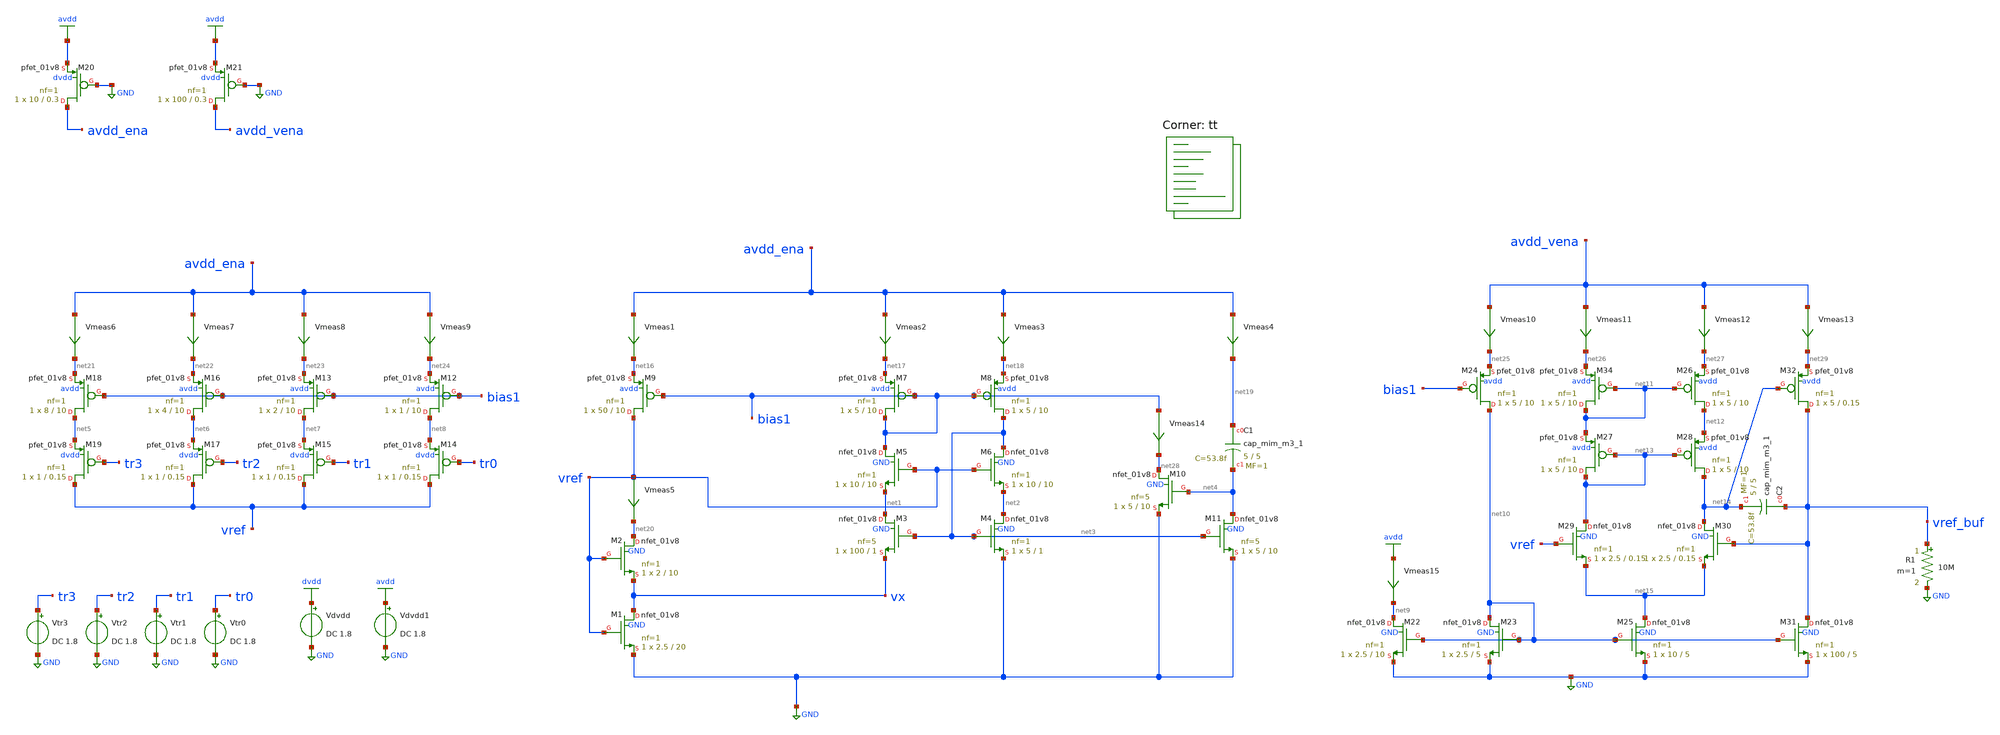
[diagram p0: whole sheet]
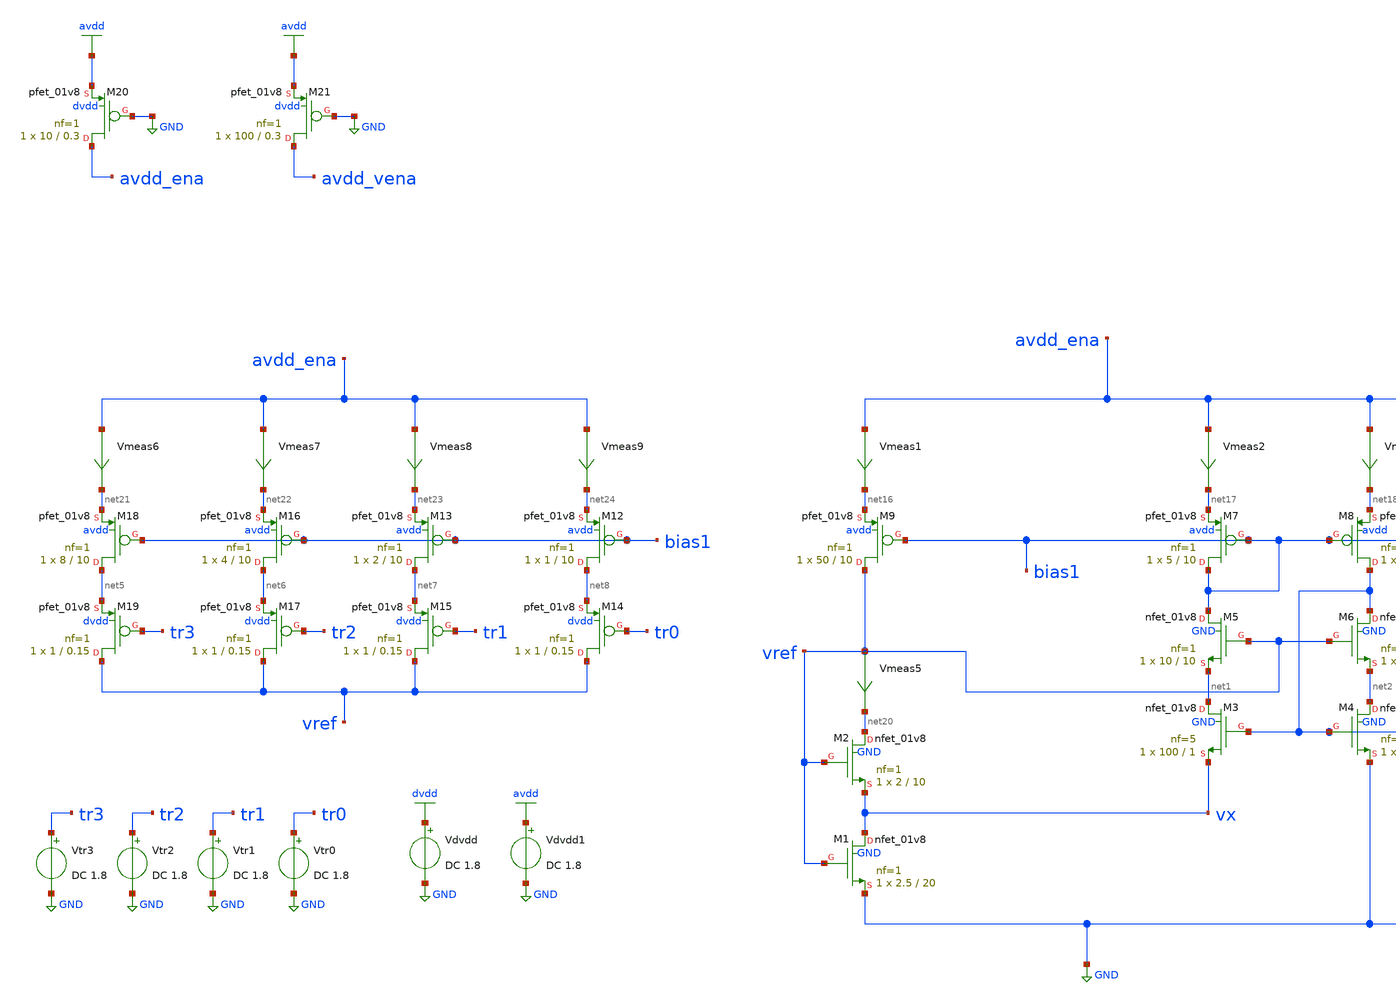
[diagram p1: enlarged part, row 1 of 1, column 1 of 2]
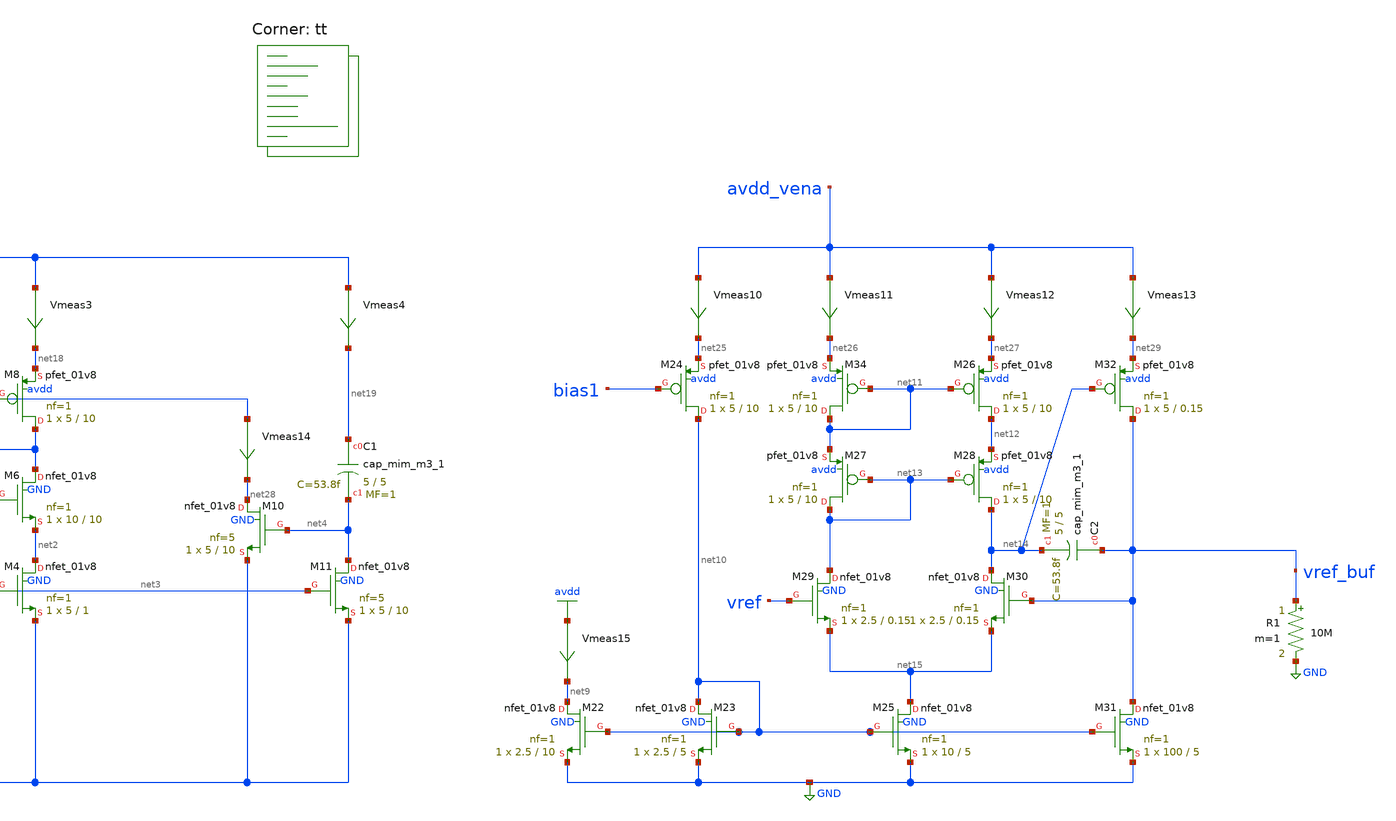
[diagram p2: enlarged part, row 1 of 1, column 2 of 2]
** sch_path: xschem/cmos_vref_design.sch
**.subckt cmos_vref_design
XM2 net20 vref vx GND sky130_fd_pr__nfet_01v8 L=10 W=2 nf=1 ad='int((nf+1)/2) * W/nf * 0.29' as='int((nf+2)/2) * W/nf * 0.29'
+ pd='2*int((nf+1)/2) * (W/nf + 0.29)' ps='2*int((nf+2)/2) * (W/nf + 0.29)' nrd='0.29 / W' nrs='0.29 / W'
+ sa=0 sb=0 sd=0 mult=1 m=1
XM1 vx vref GND GND sky130_fd_pr__nfet_01v8 L=20 W=2.5 nf=1 ad='int((nf+1)/2) * W/nf * 0.29' as='int((nf+2)/2) * W/nf * 0.29'
+ pd='2*int((nf+1)/2) * (W/nf + 0.29)' ps='2*int((nf+2)/2) * (W/nf + 0.29)' nrd='0.29 / W' nrs='0.29 / W'
+ sa=0 sb=0 sd=0 mult=1 m=1
XM3 net1 net3 vx GND sky130_fd_pr__nfet_01v8 L=1 W=100 nf=5 ad='int((nf+1)/2) * W/nf * 0.29' as='int((nf+2)/2) * W/nf * 0.29'
+ pd='2*int((nf+1)/2) * (W/nf + 0.29)' ps='2*int((nf+2)/2) * (W/nf + 0.29)' nrd='0.29 / W' nrs='0.29 / W'
+ sa=0 sb=0 sd=0 mult=1 m=1
XM4 net2 net3 GND GND sky130_fd_pr__nfet_01v8 L=1 W=5 nf=1 ad='int((nf+1)/2) * W/nf * 0.29' as='int((nf+2)/2) * W/nf * 0.29'
+ pd='2*int((nf+1)/2) * (W/nf + 0.29)' ps='2*int((nf+2)/2) * (W/nf + 0.29)' nrd='0.29 / W' nrs='0.29 / W'
+ sa=0 sb=0 sd=0 mult=1 m=1
XM5 bias1 vref net1 GND sky130_fd_pr__nfet_01v8 L=10 W=10 nf=1 ad='int((nf+1)/2) * W/nf * 0.29' as='int((nf+2)/2) * W/nf * 0.29'
+ pd='2*int((nf+1)/2) * (W/nf + 0.29)' ps='2*int((nf+2)/2) * (W/nf + 0.29)' nrd='0.29 / W' nrs='0.29 / W'
+ sa=0 sb=0 sd=0 mult=1 m=1
XM6 net3 vref net2 GND sky130_fd_pr__nfet_01v8 L=10 W=10 nf=1 ad='int((nf+1)/2) * W/nf * 0.29' as='int((nf+2)/2) * W/nf * 0.29'
+ pd='2*int((nf+1)/2) * (W/nf + 0.29)' ps='2*int((nf+2)/2) * (W/nf + 0.29)' nrd='0.29 / W' nrs='0.29 / W'
+ sa=0 sb=0 sd=0 mult=1 m=1
XM7 bias1 bias1 net17 avdd sky130_fd_pr__pfet_01v8 L=10 W=5 nf=1 ad='int((nf+1)/2) * W/nf * 0.29' as='int((nf+2)/2) * W/nf * 0.29'
+ pd='2*int((nf+1)/2) * (W/nf + 0.29)' ps='2*int((nf+2)/2) * (W/nf + 0.29)' nrd='0.29 / W' nrs='0.29 / W'
+ sa=0 sb=0 sd=0 mult=1 m=1
XM8 net3 bias1 net18 avdd sky130_fd_pr__pfet_01v8 L=10 W=5 nf=1 ad='int((nf+1)/2) * W/nf * 0.29' as='int((nf+2)/2) * W/nf * 0.29'
+ pd='2*int((nf+1)/2) * (W/nf + 0.29)' ps='2*int((nf+2)/2) * (W/nf + 0.29)' nrd='0.29 / W' nrs='0.29 / W'
+ sa=0 sb=0 sd=0 mult=1 m=1
XM9 vref bias1 net16 avdd sky130_fd_pr__pfet_01v8 L=10 W=50 nf=1 ad='int((nf+1)/2) * W/nf * 0.29' as='int((nf+2)/2) * W/nf * 0.29'
+ pd='2*int((nf+1)/2) * (W/nf + 0.29)' ps='2*int((nf+2)/2) * (W/nf + 0.29)' nrd='0.29 / W' nrs='0.29 / W'
+ sa=0 sb=0 sd=0 mult=1 m=1
XM12 net8 bias1 net24 avdd sky130_fd_pr__pfet_01v8 L=10 W=1 nf=1 ad='int((nf+1)/2) * W/nf * 0.29' as='int((nf+2)/2) * W/nf * 0.29'
+ pd='2*int((nf+1)/2) * (W/nf + 0.29)' ps='2*int((nf+2)/2) * (W/nf + 0.29)' nrd='0.29 / W' nrs='0.29 / W'
+ sa=0 sb=0 sd=0 mult=1 m=1
XM13 net7 bias1 net23 avdd sky130_fd_pr__pfet_01v8 L=10 W=2 nf=1 ad='int((nf+1)/2) * W/nf * 0.29' as='int((nf+2)/2) * W/nf * 0.29'
+ pd='2*int((nf+1)/2) * (W/nf + 0.29)' ps='2*int((nf+2)/2) * (W/nf + 0.29)' nrd='0.29 / W' nrs='0.29 / W'
+ sa=0 sb=0 sd=0 mult=1 m=1
XM14 vref tr0 net8 dvdd sky130_fd_pr__pfet_01v8 L=0.15 W=1 nf=1 ad='int((nf+1)/2) * W/nf * 0.29' as='int((nf+2)/2) * W/nf * 0.29'
+ pd='2*int((nf+1)/2) * (W/nf + 0.29)' ps='2*int((nf+2)/2) * (W/nf + 0.29)' nrd='0.29 / W' nrs='0.29 / W'
+ sa=0 sb=0 sd=0 mult=1 m=1
XM15 vref tr1 net7 dvdd sky130_fd_pr__pfet_01v8 L=0.15 W=1 nf=1 ad='int((nf+1)/2) * W/nf * 0.29' as='int((nf+2)/2) * W/nf * 0.29'
+ pd='2*int((nf+1)/2) * (W/nf + 0.29)' ps='2*int((nf+2)/2) * (W/nf + 0.29)' nrd='0.29 / W' nrs='0.29 / W'
+ sa=0 sb=0 sd=0 mult=1 m=1
XM16 net6 bias1 net22 avdd sky130_fd_pr__pfet_01v8 L=10 W=4 nf=1 ad='int((nf+1)/2) * W/nf * 0.29' as='int((nf+2)/2) * W/nf * 0.29'
+ pd='2*int((nf+1)/2) * (W/nf + 0.29)' ps='2*int((nf+2)/2) * (W/nf + 0.29)' nrd='0.29 / W' nrs='0.29 / W'
+ sa=0 sb=0 sd=0 mult=1 m=1
XM17 vref tr2 net6 dvdd sky130_fd_pr__pfet_01v8 L=0.15 W=1 nf=1 ad='int((nf+1)/2) * W/nf * 0.29' as='int((nf+2)/2) * W/nf * 0.29'
+ pd='2*int((nf+1)/2) * (W/nf + 0.29)' ps='2*int((nf+2)/2) * (W/nf + 0.29)' nrd='0.29 / W' nrs='0.29 / W'
+ sa=0 sb=0 sd=0 mult=1 m=1
XM18 net5 bias1 net21 avdd sky130_fd_pr__pfet_01v8 L=10 W=8 nf=1 ad='int((nf+1)/2) * W/nf * 0.29' as='int((nf+2)/2) * W/nf * 0.29'
+ pd='2*int((nf+1)/2) * (W/nf + 0.29)' ps='2*int((nf+2)/2) * (W/nf + 0.29)' nrd='0.29 / W' nrs='0.29 / W'
+ sa=0 sb=0 sd=0 mult=1 m=1
XM19 vref tr3 net5 dvdd sky130_fd_pr__pfet_01v8 L=0.15 W=1 nf=1 ad='int((nf+1)/2) * W/nf * 0.29' as='int((nf+2)/2) * W/nf * 0.29'
+ pd='2*int((nf+1)/2) * (W/nf + 0.29)' ps='2*int((nf+2)/2) * (W/nf + 0.29)' nrd='0.29 / W' nrs='0.29 / W'
+ sa=0 sb=0 sd=0 mult=1 m=1
XM20 avdd_ena GND avdd dvdd sky130_fd_pr__pfet_01v8 L=0.3 W=10 nf=1 ad='int((nf+1)/2) * W/nf * 0.29'
+ as='int((nf+2)/2) * W/nf * 0.29' pd='2*int((nf+1)/2) * (W/nf + 0.29)' ps='2*int((nf+2)/2) * (W/nf + 0.29)'
+ nrd='0.29 / W' nrs='0.29 / W' sa=0 sb=0 sd=0 mult=1 m=1
XM21 avdd_vena GND avdd dvdd sky130_fd_pr__pfet_01v8 L=0.3 W=100 nf=1 ad='int((nf+1)/2) * W/nf * 0.29'
+ as='int((nf+2)/2) * W/nf * 0.29' pd='2*int((nf+1)/2) * (W/nf + 0.29)' ps='2*int((nf+2)/2) * (W/nf + 0.29)'
+ nrd='0.29 / W' nrs='0.29 / W' sa=0 sb=0 sd=0 mult=1 m=1
XM22 net9 net10 GND GND sky130_fd_pr__nfet_01v8 L=10 W=2.5 nf=1 ad='int((nf+1)/2) * W/nf * 0.29' as='int((nf+2)/2) * W/nf * 0.29'
+ pd='2*int((nf+1)/2) * (W/nf + 0.29)' ps='2*int((nf+2)/2) * (W/nf + 0.29)' nrd='0.29 / W' nrs='0.29 / W'
+ sa=0 sb=0 sd=0 mult=1 m=1
XM23 net10 net10 GND GND sky130_fd_pr__nfet_01v8 L=5 W=2.5 nf=1 ad='int((nf+1)/2) * W/nf * 0.29' as='int((nf+2)/2) * W/nf * 0.29'
+ pd='2*int((nf+1)/2) * (W/nf + 0.29)' ps='2*int((nf+2)/2) * (W/nf + 0.29)' nrd='0.29 / W' nrs='0.29 / W'
+ sa=0 sb=0 sd=0 mult=1 m=1
XM24 net10 bias1 net25 avdd sky130_fd_pr__pfet_01v8 L=10 W=5 nf=1 ad='int((nf+1)/2) * W/nf * 0.29' as='int((nf+2)/2) * W/nf * 0.29'
+ pd='2*int((nf+1)/2) * (W/nf + 0.29)' ps='2*int((nf+2)/2) * (W/nf + 0.29)' nrd='0.29 / W' nrs='0.29 / W'
+ sa=0 sb=0 sd=0 mult=1 m=1
XM25 net15 net10 GND GND sky130_fd_pr__nfet_01v8 L=5 W=10 nf=1 ad='int((nf+1)/2) * W/nf * 0.29' as='int((nf+2)/2) * W/nf * 0.29'
+ pd='2*int((nf+1)/2) * (W/nf + 0.29)' ps='2*int((nf+2)/2) * (W/nf + 0.29)' nrd='0.29 / W' nrs='0.29 / W'
+ sa=0 sb=0 sd=0 mult=1 m=1
XM26 net12 net11 net27 avdd sky130_fd_pr__pfet_01v8 L=10 W=5 nf=1 ad='int((nf+1)/2) * W/nf * 0.29' as='int((nf+2)/2) * W/nf * 0.29'
+ pd='2*int((nf+1)/2) * (W/nf + 0.29)' ps='2*int((nf+2)/2) * (W/nf + 0.29)' nrd='0.29 / W' nrs='0.29 / W'
+ sa=0 sb=0 sd=0 mult=1 m=1
XM27 net13 net13 net11 avdd sky130_fd_pr__pfet_01v8 L=10 W=5 nf=1 ad='int((nf+1)/2) * W/nf * 0.29' as='int((nf+2)/2) * W/nf * 0.29'
+ pd='2*int((nf+1)/2) * (W/nf + 0.29)' ps='2*int((nf+2)/2) * (W/nf + 0.29)' nrd='0.29 / W' nrs='0.29 / W'
+ sa=0 sb=0 sd=0 mult=1 m=1
XM28 net14 net13 net12 avdd sky130_fd_pr__pfet_01v8 L=10 W=5 nf=1 ad='int((nf+1)/2) * W/nf * 0.29' as='int((nf+2)/2) * W/nf * 0.29'
+ pd='2*int((nf+1)/2) * (W/nf + 0.29)' ps='2*int((nf+2)/2) * (W/nf + 0.29)' nrd='0.29 / W' nrs='0.29 / W'
+ sa=0 sb=0 sd=0 mult=1 m=1
XM29 net13 vref net15 GND sky130_fd_pr__nfet_01v8 L=0.15 W=2.5 nf=1 ad='int((nf+1)/2) * W/nf * 0.29'
+ as='int((nf+2)/2) * W/nf * 0.29' pd='2*int((nf+1)/2) * (W/nf + 0.29)' ps='2*int((nf+2)/2) * (W/nf + 0.29)'
+ nrd='0.29 / W' nrs='0.29 / W' sa=0 sb=0 sd=0 mult=1 m=1
XM30 net14 vref_buf net15 GND sky130_fd_pr__nfet_01v8 L=0.15 W=2.5 nf=1 ad='int((nf+1)/2) * W/nf * 0.29'
+ as='int((nf+2)/2) * W/nf * 0.29' pd='2*int((nf+1)/2) * (W/nf + 0.29)' ps='2*int((nf+2)/2) * (W/nf + 0.29)'
+ nrd='0.29 / W' nrs='0.29 / W' sa=0 sb=0 sd=0 mult=1 m=1
XM34 net11 net11 net26 avdd sky130_fd_pr__pfet_01v8 L=10 W=5 nf=1 ad='int((nf+1)/2) * W/nf * 0.29' as='int((nf+2)/2) * W/nf * 0.29'
+ pd='2*int((nf+1)/2) * (W/nf + 0.29)' ps='2*int((nf+2)/2) * (W/nf + 0.29)' nrd='0.29 / W' nrs='0.29 / W'
+ sa=0 sb=0 sd=0 mult=1 m=1
XM10 net28 net4 GND GND sky130_fd_pr__nfet_01v8 L=10 W=5 nf=5 ad='int((nf+1)/2) * W/nf * 0.29' as='int((nf+2)/2) * W/nf * 0.29'
+ pd='2*int((nf+1)/2) * (W/nf + 0.29)' ps='2*int((nf+2)/2) * (W/nf + 0.29)' nrd='0.29 / W' nrs='0.29 / W'
+ sa=0 sb=0 sd=0 mult=1 m=1
XM11 net4 net3 GND GND sky130_fd_pr__nfet_01v8 L=10 W=5 nf=5 ad='int((nf+1)/2) * W/nf * 0.29' as='int((nf+2)/2) * W/nf * 0.29'
+ pd='2*int((nf+1)/2) * (W/nf + 0.29)' ps='2*int((nf+2)/2) * (W/nf + 0.29)' nrd='0.29 / W' nrs='0.29 / W'
+ sa=0 sb=0 sd=0 mult=1 m=1
XC1 net19 net4 sky130_fd_pr__cap_mim_m3_1 W=5 L=5 MF=1 m=1
Vmeas1 avdd_ena net16 0
.save i(vmeas1)
Vmeas2 avdd_ena net17 0
.save i(vmeas2)
Vmeas3 avdd_ena net18 0
.save i(vmeas3)
Vmeas4 avdd_ena net19 0
.save i(vmeas4)
Vmeas5 vref net20 0
.save i(vmeas5)
Vmeas6 avdd_ena net21 0
.save i(vmeas6)
Vmeas7 avdd_ena net22 0
.save i(vmeas7)
Vmeas8 avdd_ena net23 0
.save i(vmeas8)
Vmeas9 avdd_ena net24 0
.save i(vmeas9)
Vmeas10 avdd_vena net25 0
.save i(vmeas10)
Vmeas11 avdd_vena net26 0
.save i(vmeas11)
Vmeas12 avdd_vena net27 0
.save i(vmeas12)
Vmeas13 avdd_vena net29 0
.save i(vmeas13)
Vdvdd dvdd GND DC 1.8
Vdvdd1 avdd GND DC 1.8
Vtr0 tr0 GND DC 1.8
Vtr1 tr1 GND DC 1.8
Vtr2 tr2 GND DC 1.8
Vtr3 tr3 GND DC 1.8
Vmeas14 bias1 net28 0
.save i(vmeas14)
R1 vref_buf GND 10M m=1
XM31 vref_buf net10 GND GND sky130_fd_pr__nfet_01v8 L=5 W=100 nf=1 ad='int((nf+1)/2) * W/nf * 0.29' as='int((nf+2)/2) * W/nf * 0.29'
+ pd='2*int((nf+1)/2) * (W/nf + 0.29)' ps='2*int((nf+2)/2) * (W/nf + 0.29)' nrd='0.29 / W' nrs='0.29 / W'
+ sa=0 sb=0 sd=0 mult=1 m=1
XC2 vref_buf net14 sky130_fd_pr__cap_mim_m3_1 W=5 L=5 MF=1 m=1
XM32 vref_buf net14 net29 avdd sky130_fd_pr__pfet_01v8 L=0.15 W=5 nf=1 ad='int((nf+1)/2) * W/nf * 0.29'
+ as='int((nf+2)/2) * W/nf * 0.29' pd='2*int((nf+1)/2) * (W/nf + 0.29)' ps='2*int((nf+2)/2) * (W/nf + 0.29)'
+ nrd='0.29 / W' nrs='0.29 / W' sa=0 sb=0 sd=0 mult=1 m=1
Vmeas15 avdd net9 0
.save i(vmeas15)
**** begin user architecture code
.lib $::SKYWATER_MODELS/sky130.lib.spice tt


.option warn=1
.control
save vref, vref_buf, bias1
dc TEMP -40 85 5
plot i(vmeas10), i(vmeas11), i(vmeas12)
plot vref_buf, vref
.endc


**** end user architecture code
**.ends
.GLOBAL GND
.GLOBAL avdd
.GLOBAL dvdd
.end
